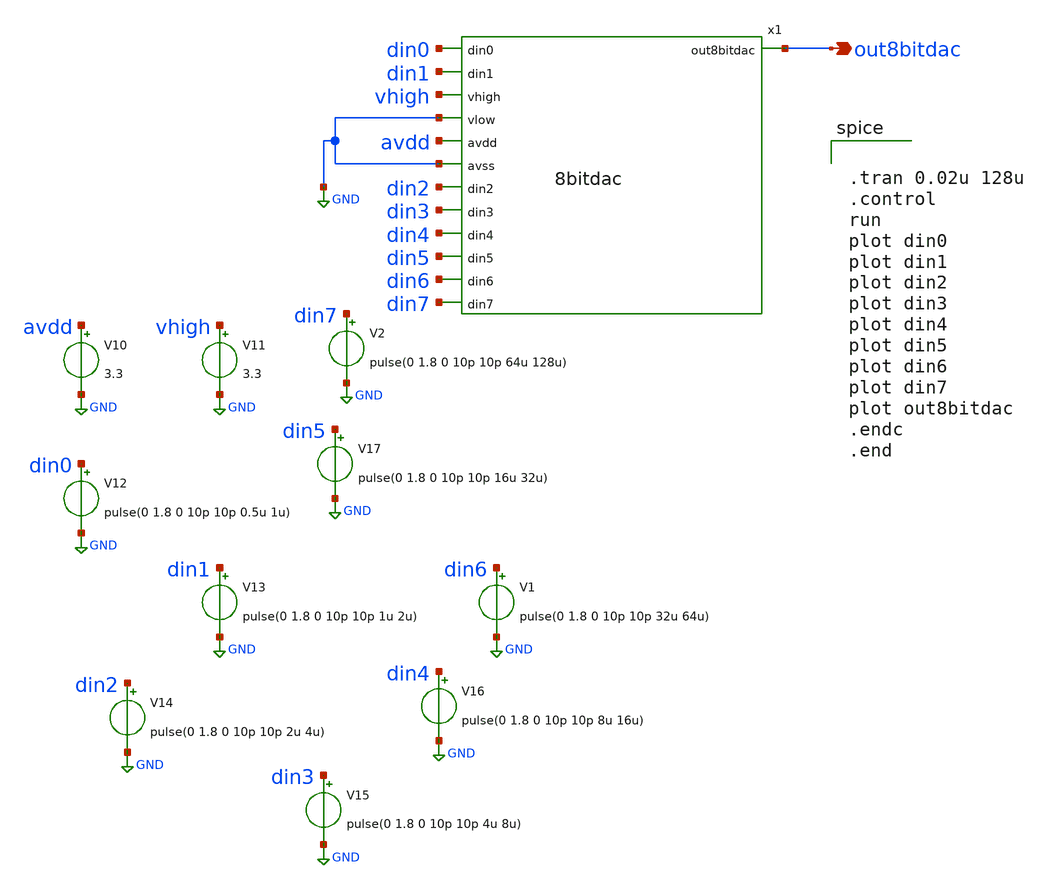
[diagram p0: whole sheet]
** sch_path: xschem/tb_8bitdac.sch
**.subckt tb_8bitdac out8bitdac
*.opin out8bitdac
x1 out8bitdac din0 din1 vhigh GND avdd GND din2 din3 din4 din5 din6 din7 8bitdac
V10 avdd GND 3.3
V11 vhigh GND 3.3
V12 din0 GND pulse(0 1.8 0 10p 10p 0.5u 1u)
V13 din1 GND pulse(0 1.8 0 10p 10p 1u 2u)
V14 din2 GND pulse(0 1.8 0 10p 10p 2u 4u)
V15 din3 GND pulse(0 1.8 0 10p 10p 4u 8u)
V16 din4 GND pulse(0 1.8 0 10p 10p 8u 16u)
V17 din5 GND pulse(0 1.8 0 10p 10p 16u 32u)
V1 din6 GND pulse(0 1.8 0 10p 10p 32u 64u)
V2 din7 GND pulse(0 1.8 0 10p 10p 64u 128u)
**** begin user architecture code

** opencircuitdesign pdks install
.lib $::SKYWATER_MODELS/sky130.lib.spice tt




.tran 0.02u 128u
.control
run
plot din0
plot din1
plot din2
plot din3
plot din4
plot din5
plot din6
plot din7
plot out8bitdac
.endc
.end

**** end user architecture code
**.ends
.GLOBAL GND
.end
